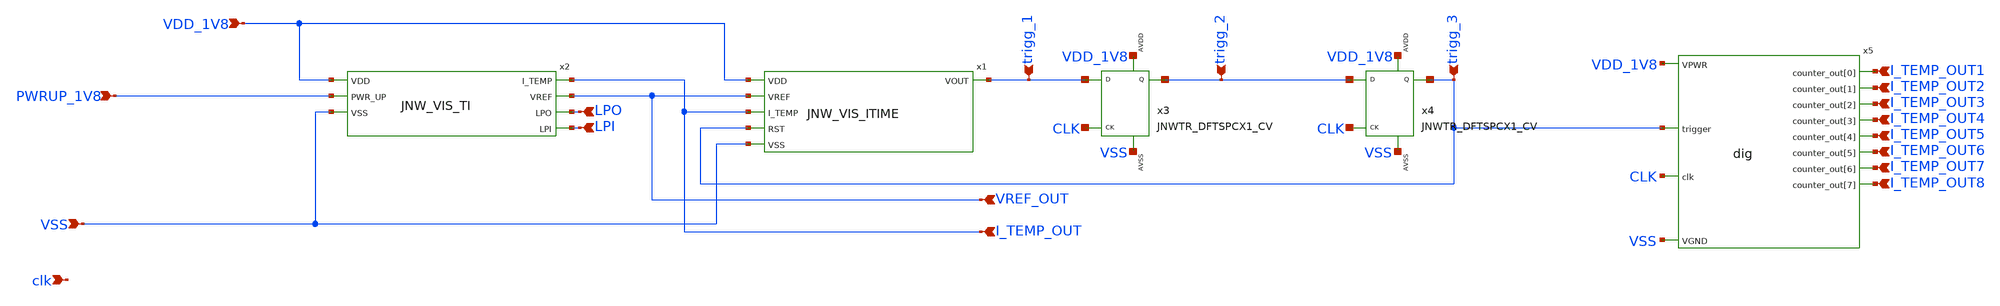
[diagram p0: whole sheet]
** sch_path: design/JNW_GR02_SKY130A/JNW_GR02_dig.sch
**.subckt JNW_GR02_dig VDD_1V8 VSS PWRUP_1V8 I_TEMP_OUT LPI LPO VREF_OUT I_TEMP_OUT8 I_TEMP_OUT7
*+ I_TEMP_OUT6 I_TEMP_OUT5 I_TEMP_OUT4 I_TEMP_OUT3 I_TEMP_OUT2 I_TEMP_OUT1 trigg_1 trigg_2 trigg_3 clk
*.ipin VDD_1V8
*.ipin VSS
*.ipin PWRUP_1V8
*.ipin I_TEMP_OUT
*.ipin LPI
*.ipin LPO
*.ipin VREF_OUT
*.ipin I_TEMP_OUT8
*.ipin I_TEMP_OUT7
*.ipin I_TEMP_OUT6
*.ipin I_TEMP_OUT5
*.ipin I_TEMP_OUT4
*.ipin I_TEMP_OUT3
*.ipin I_TEMP_OUT2
*.ipin I_TEMP_OUT1
*.ipin trigg_1
*.ipin trigg_2
*.ipin trigg_3
*.ipin clk
x1 VDD_1V8 VREF_OUT trigg_1 I_TEMP_OUT trigg_3 VSS JNW_VIS_ITIME
x2 I_TEMP_OUT VDD_1V8 VREF_OUT LPO LPI PWRUP_1V8 VSS JNW_VIS_TI
x3 trigg_1 CLK trigg_2 VDD_1V8 VSS JNWTR_DFTSPCX1_CV xoffset=0 yoffset=0 angle=0
x4 trigg_2 CLK trigg_3 VDD_1V8 VSS JNWTR_DFTSPCX1_CV xoffset=0 yoffset=0 angle=0
x5 VSS VDD_1V8 CLK I_TEMP_OUT1 I_TEMP_OUT2 I_TEMP_OUT3 I_TEMP_OUT4 I_TEMP_OUT5 I_TEMP_OUT6
+ I_TEMP_OUT7 I_TEMP_OUT8 trigg_3 dig
**** begin user architecture code



.include /home/georg/aicex/ip/jnw_gr02_sky130a/design/JNW_GR02_SKY130A/dig.spice




**** end user architecture code
**.ends
.end
